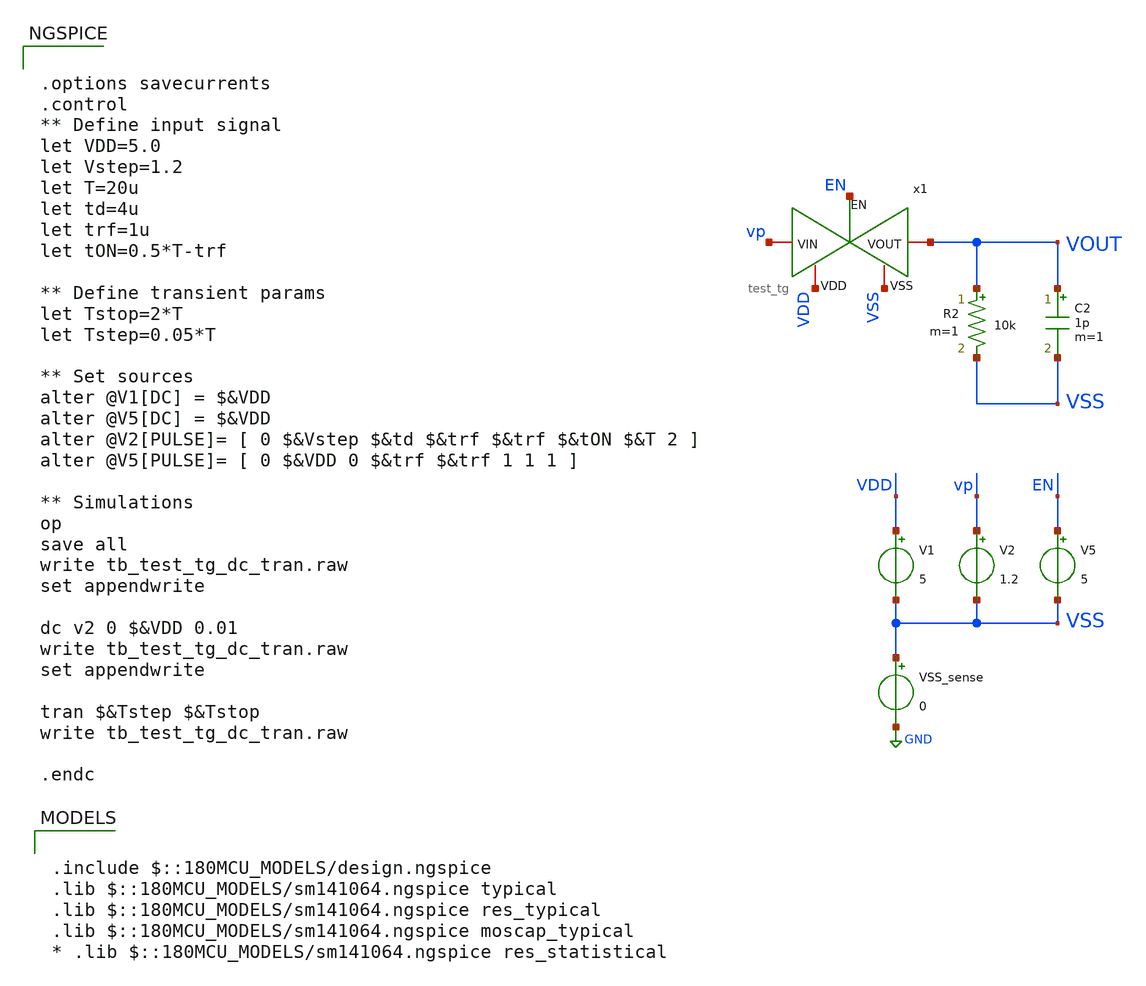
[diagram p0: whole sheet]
** sch_path: designs/libs/tb_test/tb_test_tg/tb_test_tg.sch
**.subckt tb_test_tg
x1 VDD EN vp VOUT VSS test_tg
V1 VDD VSS 5
V2 vp VSS 1.2
VSS_sense VSS GND 0
V5 EN VSS 5
C2 VOUT VSS 1p m=1
R2 VOUT VSS 10k m=1
**** begin user architecture code

.include $::180MCU_MODELS/design.ngspice
.lib $::180MCU_MODELS/sm141064.ngspice typical
.lib $::180MCU_MODELS/sm141064.ngspice res_typical
.lib $::180MCU_MODELS/sm141064.ngspice moscap_typical
* .lib $::180MCU_MODELS/sm141064.ngspice res_statistical



.options savecurrents
.control
** Define input signal
let VDD=5.0
let Vstep=1.2
let T=20u
let td=4u
let trf=1u
let tON=0.5*T-trf

** Define transient params
let Tstop=2*T
let Tstep=0.05*T

** Set sources
alter @V1[DC] = $&VDD
alter @V5[DC] = $&VDD
alter @V2[PULSE]= [ 0 $&Vstep $&td $&trf $&trf $&tON $&T 2 ]
alter @V5[PULSE]= [ 0 $&VDD 0 $&trf $&trf 1 1 1 ]

** Simulations
op
save all
write tb_test_tg_dc_tran.raw
set appendwrite

dc v2 0 $&VDD 0.01
write tb_test_tg_dc_tran.raw
set appendwrite

tran $&Tstep $&Tstop
write tb_test_tg_dc_tran.raw

.endc


**** end user architecture code
**.ends

* expanding   symbol:  libs/core_test/test_tg/test_tg.sym # of pins=5
** sym_path: designs/libs/core_test/test_tg/test_tg.sym
** sch_path: designs/libs/core_test/test_tg/test_tg.sch
.subckt test_tg VDD EN VIN VOUT VSS
*.iopin VIN
*.iopin VOUT
*.ipin EN
*.iopin VDD
*.iopin VSS
XM1 VIN EN VOUT VSS nfet_05v0 L=0.60u W=1.5u nf=1 ad='int((nf+1)/2) * W/nf * 0.18u' as='int((nf+2)/2) * W/nf * 0.18u'
+ pd='2*int((nf+1)/2) * (W/nf + 0.18u)' ps='2*int((nf+2)/2) * (W/nf + 0.18u)' nrd='0.18u / W' nrs='0.18u / W'
+ sa=0 sb=0 sd=0 m=2
XM2 VOUT ENB VIN VDD pfet_05v0 L=0.50u W=1.5u nf=1 ad='int((nf+1)/2) * W/nf * 0.18u' as='int((nf+2)/2) * W/nf * 0.18u'
+ pd='2*int((nf+1)/2) * (W/nf + 0.18u)' ps='2*int((nf+2)/2) * (W/nf + 0.18u)' nrd='0.18u / W' nrs='0.18u / W'
+ sa=0 sb=0 sd=0 m=6
x1 VDD ENB EN VSS test_inv
.ends


* expanding   symbol:  libs/core_test/test_inv/test_inv.sym # of pins=4
** sym_path: designs/libs/core_test/test_inv/test_inv.sym
** sch_path: designs/libs/core_test/test_inv/test_inv.sch
.subckt test_inv VDD OUT IN VSS
*.opin OUT
*.ipin IN
*.iopin VDD
*.iopin VSS
XM1 OUT IN VSS VSS nfet_05v0 L=0.60u W=0.30u nf=1 ad='int((nf+1)/2) * W/nf * 0.18u' as='int((nf+2)/2) * W/nf * 0.18u'
+ pd='2*int((nf+1)/2) * (W/nf + 0.18u)' ps='2*int((nf+2)/2) * (W/nf + 0.18u)' nrd='0.18u / W' nrs='0.18u / W'
+ sa=0 sb=0 sd=0 m=1
XM2 OUT IN VDD VDD pfet_05v0 L=0.50u W=0.30u nf=2 ad='int((nf+1)/2) * W/nf * 0.18u' as='int((nf+2)/2) * W/nf * 0.18u'
+ pd='2*int((nf+1)/2) * (W/nf + 0.18u)' ps='2*int((nf+2)/2) * (W/nf + 0.18u)' nrd='0.18u / W' nrs='0.18u / W'
+ sa=0 sb=0 sd=0 m=1
.ends

.GLOBAL GND
.end
